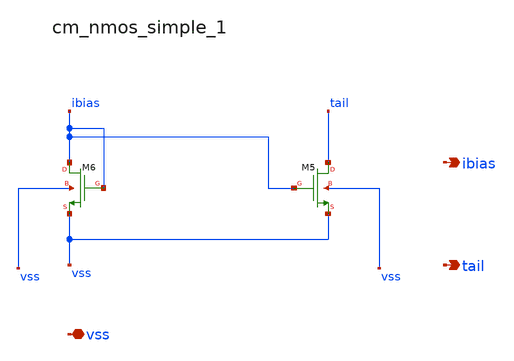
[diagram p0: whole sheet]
** sch_path: analog-db/raw/amp_001_5t/hier/blocks/cm_nmos_simple_1.sch
**.subckt cm_nmos_simple_1 vss ibias tail
*.iopin vss
*.opin ibias
*.opin tail
XM5 tail ibias vss vss sg13_lv_nmos w=x_dut_xm5_w l=x_dut_xm5_l ng=1 m=x_dut_xm5_m
XM6 ibias ibias vss vss sg13_lv_nmos w=x_dut_xm6_w l=x_dut_xm6_l ng=1 m=x_dut_xm6_m
**.ends
.end
